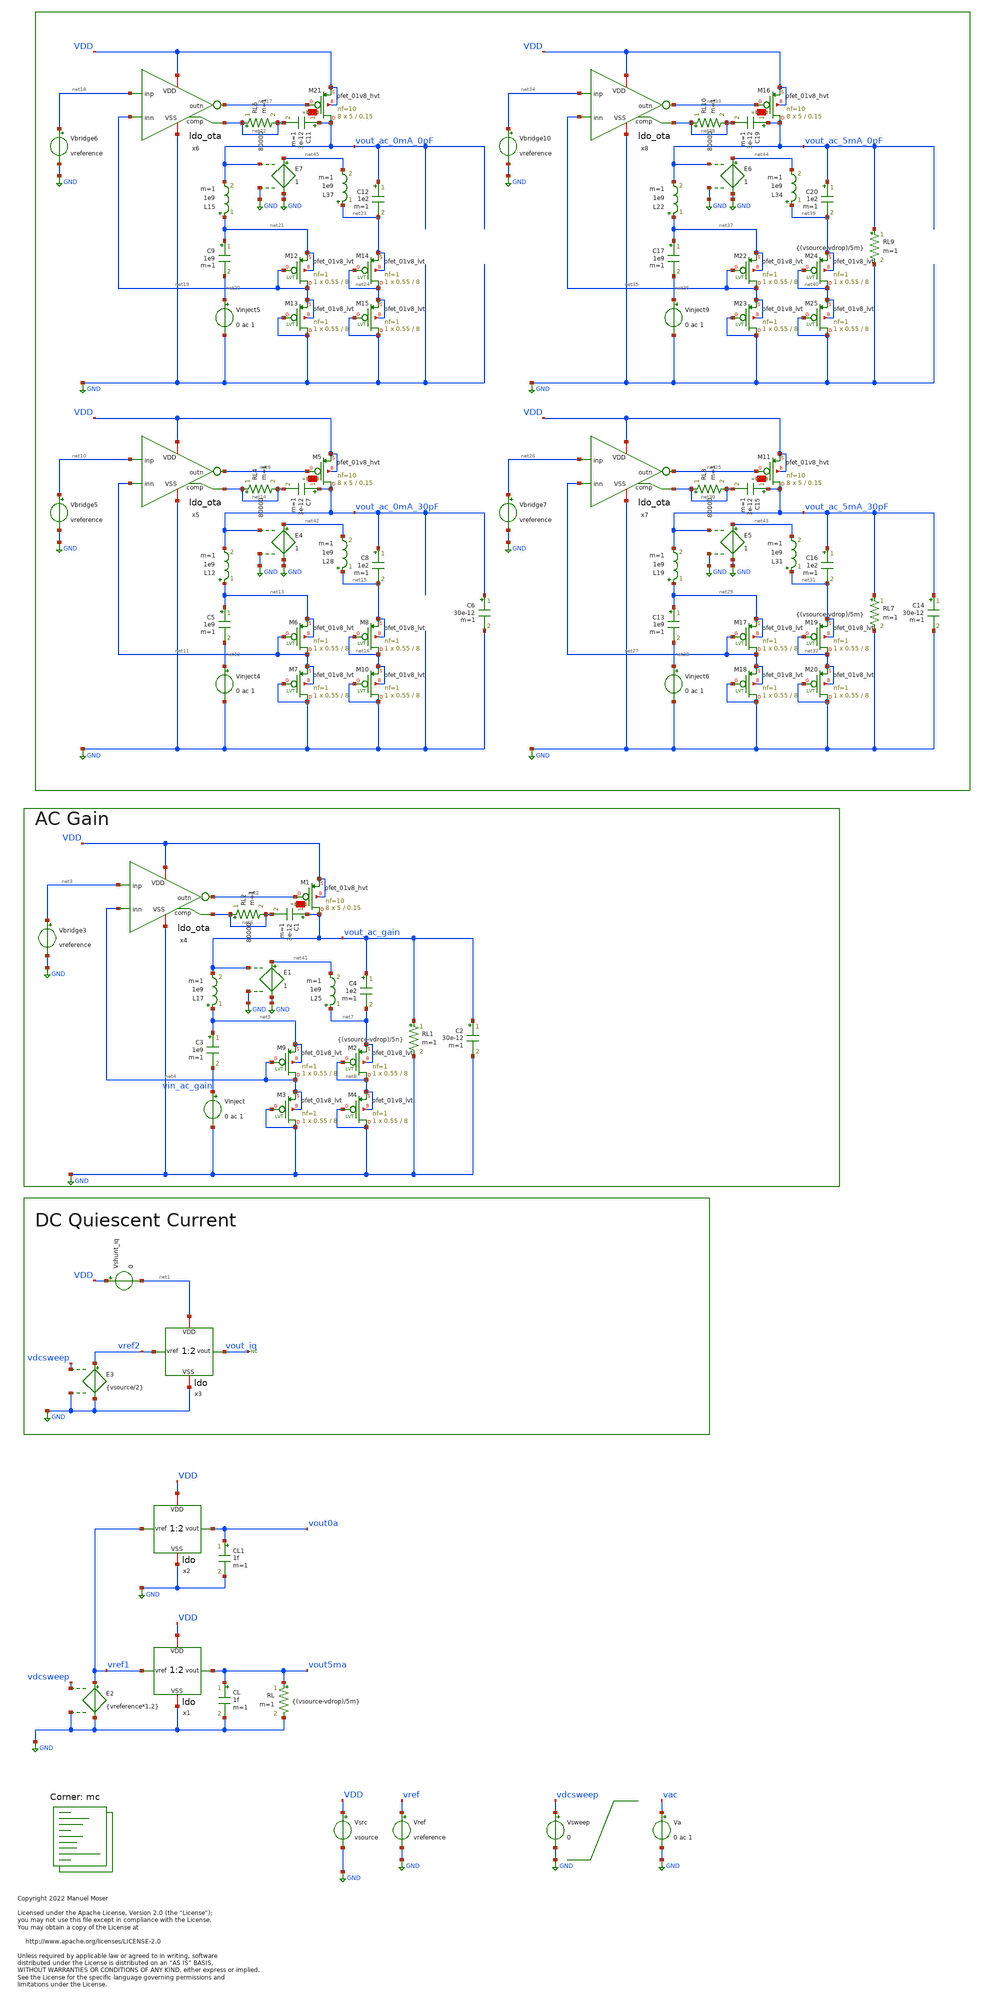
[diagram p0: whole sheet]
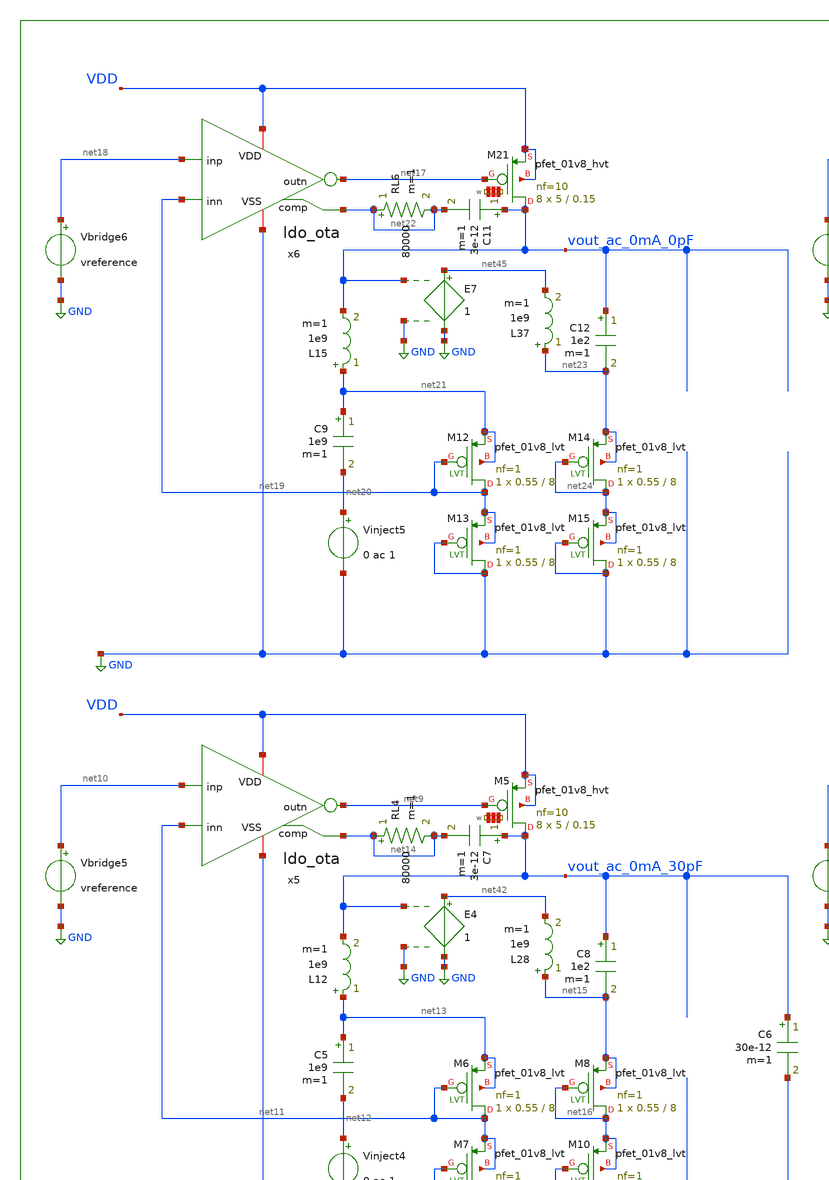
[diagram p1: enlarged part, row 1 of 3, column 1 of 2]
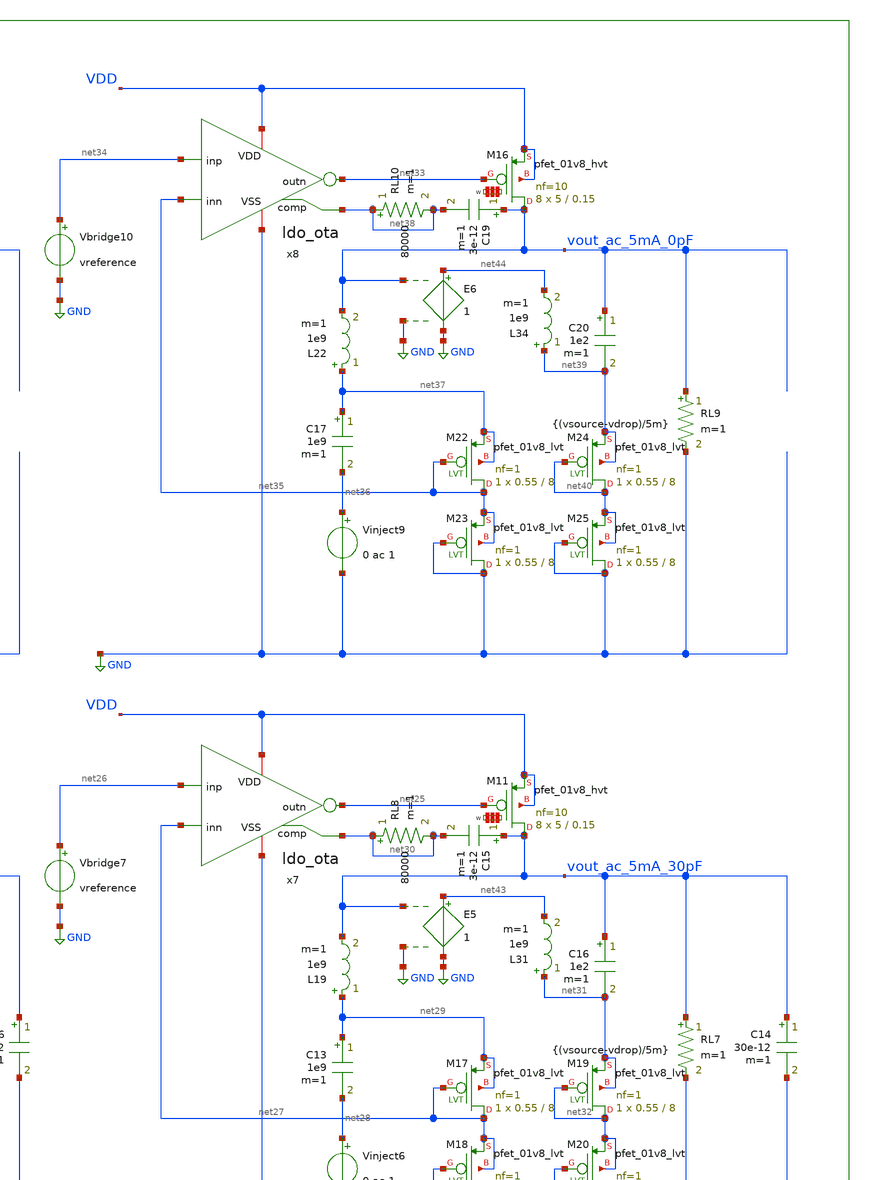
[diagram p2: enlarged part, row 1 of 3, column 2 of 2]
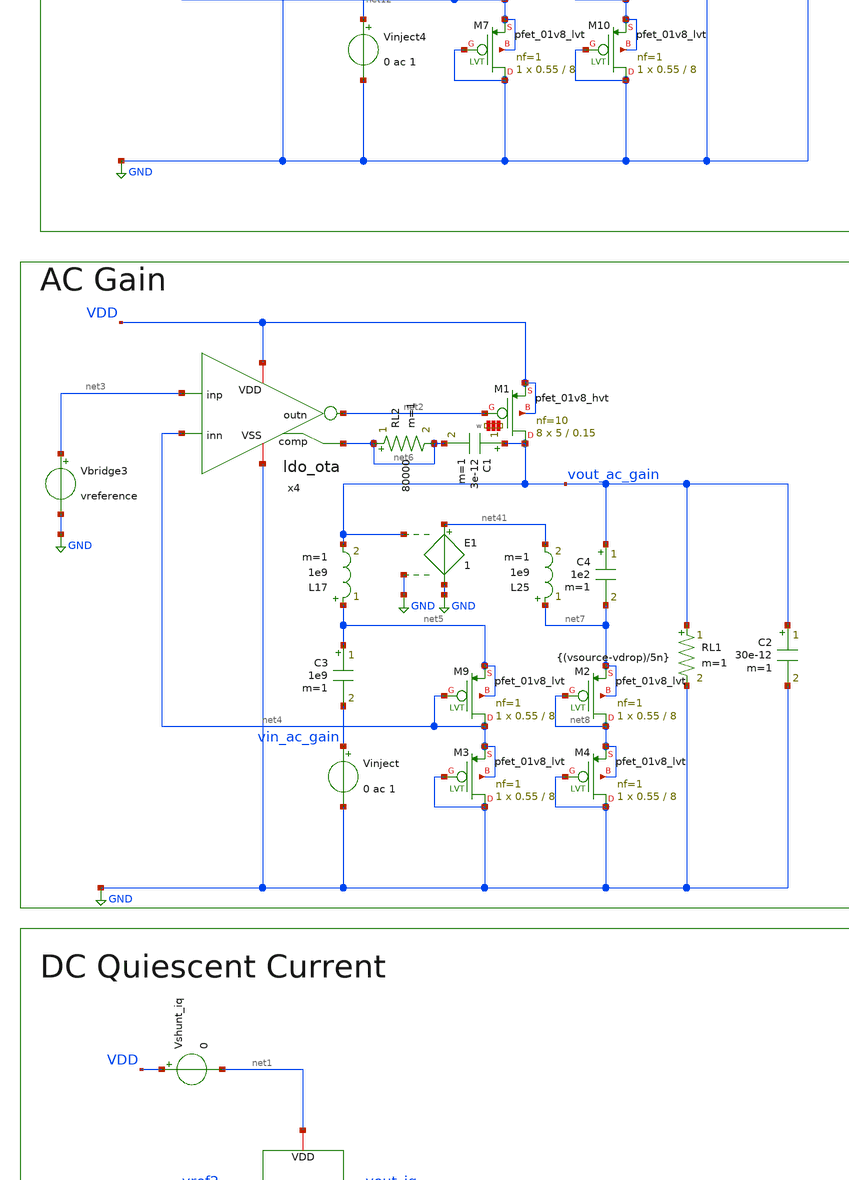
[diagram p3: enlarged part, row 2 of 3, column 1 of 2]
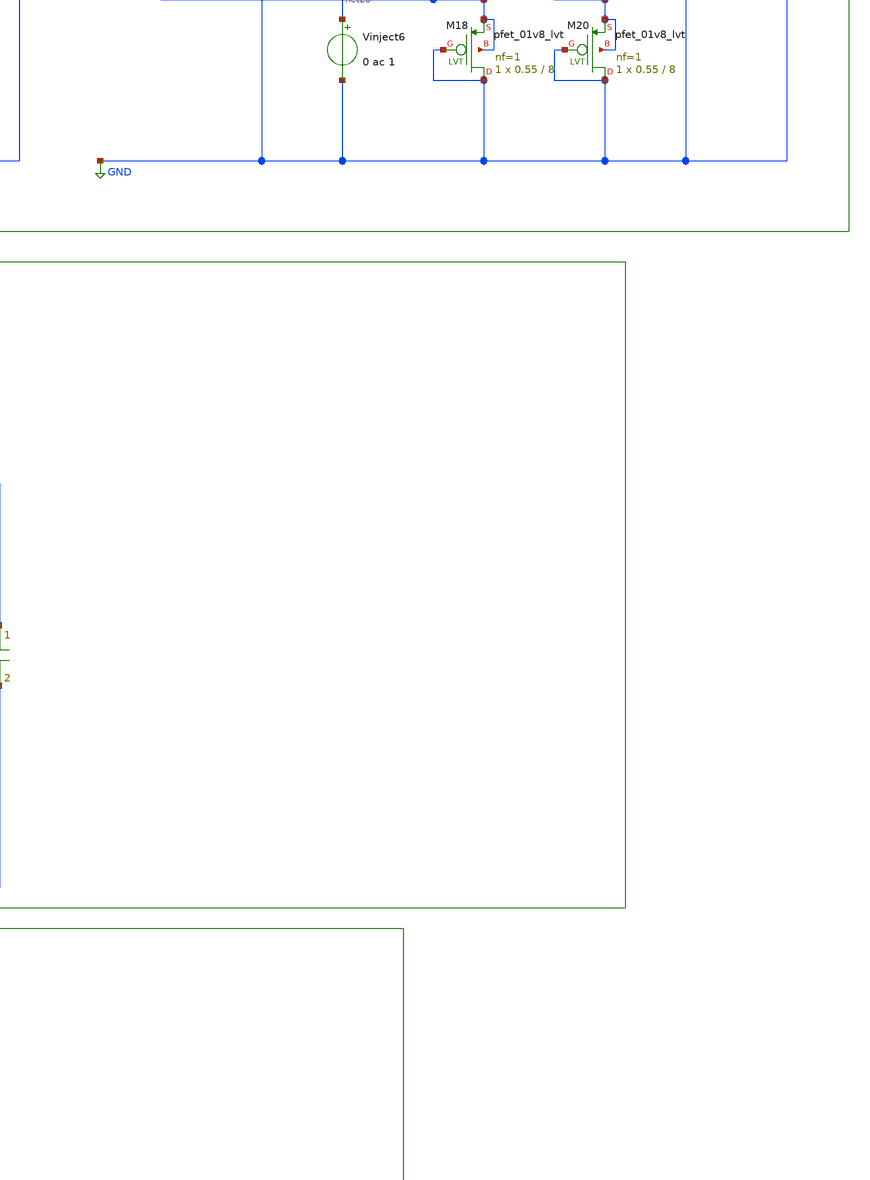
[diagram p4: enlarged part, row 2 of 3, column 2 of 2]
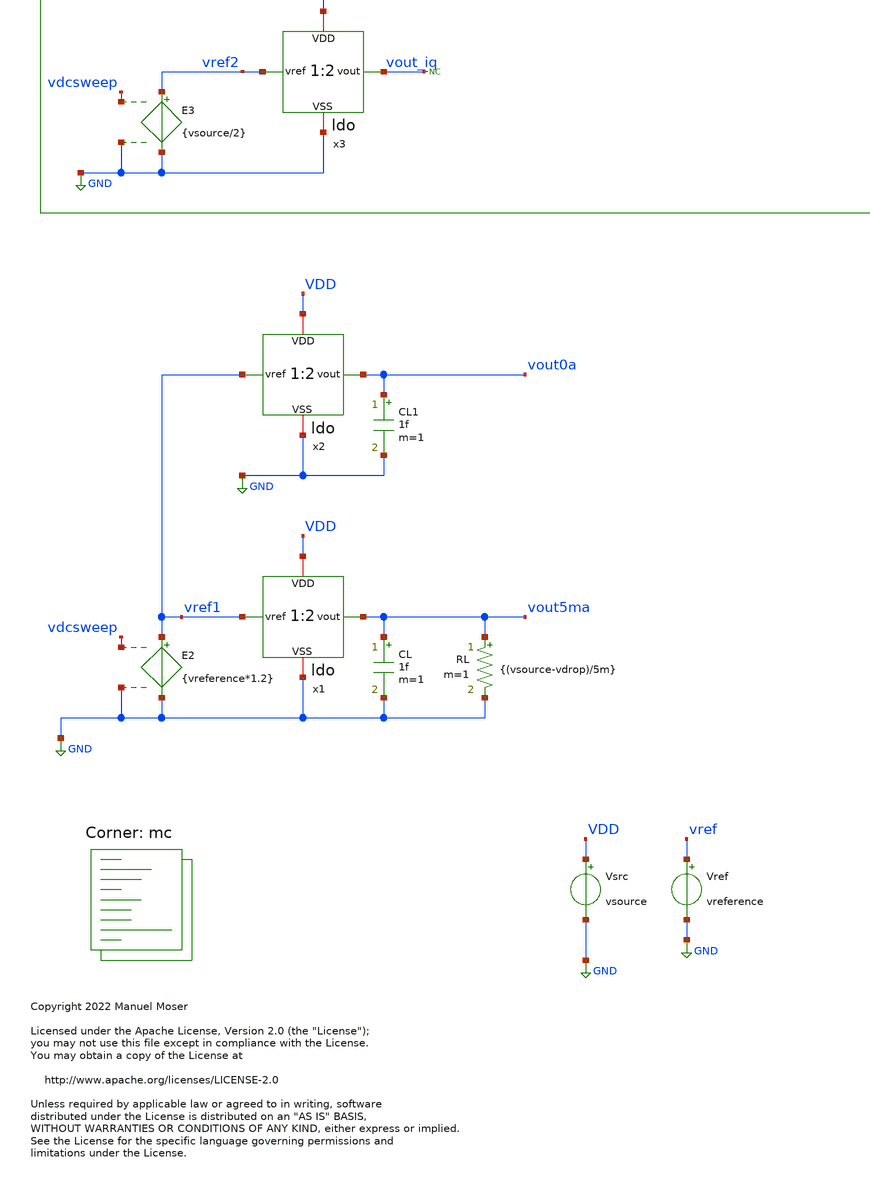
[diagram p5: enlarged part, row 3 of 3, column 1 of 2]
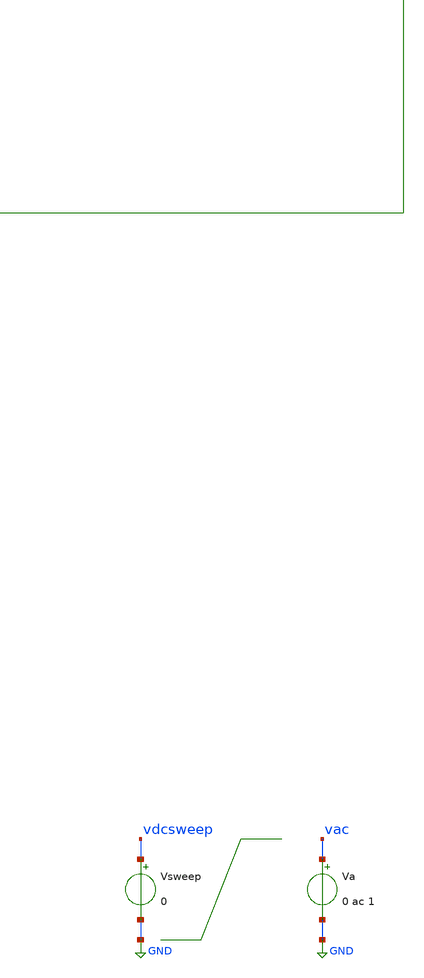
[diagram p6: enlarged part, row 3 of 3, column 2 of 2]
** sch_path: xschem/ldo_tb.sch
* Copyright 2022 Manuel Moser
* Licensed under the Apache License, Version 2.0 (the "License");
**.subckt ldo_tb
Vref vref GND vreference
Vsrc VDD GND vsource
Va vac GND 0 ac 1
CL vout5ma GND 1f m=1
RL vout5ma GND {(vsource-vdrop)/5m} m=1
x1 VDD vref1 vout5ma GND ldo
CL1 vout0a GND 1f m=1
x2 VDD vref1 vout0a GND ldo
Vsweep vdcsweep GND 0
E2 vref1 GND vdcsweep GND {vreference*1.2}
x3 net1 vref2 vout_iq GND ldo
Vshunt_iq VDD net1 0
E3 vref2 GND vdcsweep GND {vsource/2}
* noconn vout_iq
x4 VDD net3 net2 net4 GND net6 ldo_ota
L17 net5 vout_ac_gain 1e9 m=1
C3 net5 vin_ac_gain 1e9 m=1
Vinject vin_ac_gain GND 0 ac 1
Vbridge3 net3 GND vreference
RL1 vout_ac_gain GND {(vsource-vdrop)/5n} m=1
C2 vout_ac_gain GND 30e-12 m=1
C1 vout_ac_gain net6 3e-12 m=1
RL2 net6 net6 80000 m=1
XM9 net4 net4 net5 net5 sky130_fd_pr__pfet_01v8_lvt L=8 W=0.55 nf=1 ad='int((nf+1)/2) * W/nf * 0.29'
+ as='int((nf+2)/2) * W/nf * 0.29' pd='2*int((nf+1)/2) * (W/nf + 0.29)' ps='2*int((nf+2)/2) * (W/nf + 0.29)'
+ nrd='0.29 / W' nrs='0.29 / W' sa=0 sb=0 sd=0 mult=1 m=1
XM3 GND GND net4 net4 sky130_fd_pr__pfet_01v8_lvt L=8 W=0.55 nf=1 ad='int((nf+1)/2) * W/nf * 0.29' as='int((nf+2)/2) * W/nf * 0.29'
+ pd='2*int((nf+1)/2) * (W/nf + 0.29)' ps='2*int((nf+2)/2) * (W/nf + 0.29)' nrd='0.29 / W' nrs='0.29 / W'
+ sa=0 sb=0 sd=0 mult=1 m=1
XM2 net8 net8 net7 net7 sky130_fd_pr__pfet_01v8_lvt L=8 W=0.55 nf=1 ad='int((nf+1)/2) * W/nf * 0.29'
+ as='int((nf+2)/2) * W/nf * 0.29' pd='2*int((nf+1)/2) * (W/nf + 0.29)' ps='2*int((nf+2)/2) * (W/nf + 0.29)'
+ nrd='0.29 / W' nrs='0.29 / W' sa=0 sb=0 sd=0 mult=1 m=1
XM4 GND GND net8 net8 sky130_fd_pr__pfet_01v8_lvt L=8 W=0.55 nf=1 ad='int((nf+1)/2) * W/nf * 0.29' as='int((nf+2)/2) * W/nf * 0.29'
+ pd='2*int((nf+1)/2) * (W/nf + 0.29)' ps='2*int((nf+2)/2) * (W/nf + 0.29)' nrd='0.29 / W' nrs='0.29 / W'
+ sa=0 sb=0 sd=0 mult=1 m=1
C4 vout_ac_gain net7 1e2 m=1
x5 VDD net10 net9 net11 GND net14 ldo_ota
L12 net13 vout_ac_0mA_30pF 1e9 m=1
C5 net13 net12 1e9 m=1
Vinject4 net12 GND 0 ac 1
Vbridge5 net10 GND vreference
C6 vout_ac_0mA_30pF GND 30e-12 m=1
C7 vout_ac_0mA_30pF net14 3e-12 m=1
RL4 net14 net14 80000 m=1
XM6 net11 net11 net13 net13 sky130_fd_pr__pfet_01v8_lvt L=8 W=0.55 nf=1 ad='int((nf+1)/2) * W/nf * 0.29'
+ as='int((nf+2)/2) * W/nf * 0.29' pd='2*int((nf+1)/2) * (W/nf + 0.29)' ps='2*int((nf+2)/2) * (W/nf + 0.29)'
+ nrd='0.29 / W' nrs='0.29 / W' sa=0 sb=0 sd=0 mult=1 m=1
XM7 GND GND net11 net11 sky130_fd_pr__pfet_01v8_lvt L=8 W=0.55 nf=1 ad='int((nf+1)/2) * W/nf * 0.29'
+ as='int((nf+2)/2) * W/nf * 0.29' pd='2*int((nf+1)/2) * (W/nf + 0.29)' ps='2*int((nf+2)/2) * (W/nf + 0.29)'
+ nrd='0.29 / W' nrs='0.29 / W' sa=0 sb=0 sd=0 mult=1 m=1
XM8 net16 net16 net15 net15 sky130_fd_pr__pfet_01v8_lvt L=8 W=0.55 nf=1 ad='int((nf+1)/2) * W/nf * 0.29'
+ as='int((nf+2)/2) * W/nf * 0.29' pd='2*int((nf+1)/2) * (W/nf + 0.29)' ps='2*int((nf+2)/2) * (W/nf + 0.29)'
+ nrd='0.29 / W' nrs='0.29 / W' sa=0 sb=0 sd=0 mult=1 m=1
XM10 GND GND net16 net16 sky130_fd_pr__pfet_01v8_lvt L=8 W=0.55 nf=1 ad='int((nf+1)/2) * W/nf * 0.29'
+ as='int((nf+2)/2) * W/nf * 0.29' pd='2*int((nf+1)/2) * (W/nf + 0.29)' ps='2*int((nf+2)/2) * (W/nf + 0.29)'
+ nrd='0.29 / W' nrs='0.29 / W' sa=0 sb=0 sd=0 mult=1 m=1
C8 vout_ac_0mA_30pF net15 1e2 m=1
x6 VDD net18 net17 net19 GND net22 ldo_ota
L15 net21 vout_ac_0mA_0pF 1e9 m=1
C9 net21 net20 1e9 m=1
Vinject5 net20 GND 0 ac 1
Vbridge6 net18 GND vreference
C11 vout_ac_0mA_0pF net22 3e-12 m=1
RL6 net22 net22 80000 m=1
XM12 net19 net19 net21 net21 sky130_fd_pr__pfet_01v8_lvt L=8 W=0.55 nf=1 ad='int((nf+1)/2) * W/nf * 0.29'
+ as='int((nf+2)/2) * W/nf * 0.29' pd='2*int((nf+1)/2) * (W/nf + 0.29)' ps='2*int((nf+2)/2) * (W/nf + 0.29)'
+ nrd='0.29 / W' nrs='0.29 / W' sa=0 sb=0 sd=0 mult=1 m=1
XM13 GND GND net19 net19 sky130_fd_pr__pfet_01v8_lvt L=8 W=0.55 nf=1 ad='int((nf+1)/2) * W/nf * 0.29'
+ as='int((nf+2)/2) * W/nf * 0.29' pd='2*int((nf+1)/2) * (W/nf + 0.29)' ps='2*int((nf+2)/2) * (W/nf + 0.29)'
+ nrd='0.29 / W' nrs='0.29 / W' sa=0 sb=0 sd=0 mult=1 m=1
XM14 net24 net24 net23 net23 sky130_fd_pr__pfet_01v8_lvt L=8 W=0.55 nf=1 ad='int((nf+1)/2) * W/nf * 0.29'
+ as='int((nf+2)/2) * W/nf * 0.29' pd='2*int((nf+1)/2) * (W/nf + 0.29)' ps='2*int((nf+2)/2) * (W/nf + 0.29)'
+ nrd='0.29 / W' nrs='0.29 / W' sa=0 sb=0 sd=0 mult=1 m=1
XM15 GND GND net24 net24 sky130_fd_pr__pfet_01v8_lvt L=8 W=0.55 nf=1 ad='int((nf+1)/2) * W/nf * 0.29'
+ as='int((nf+2)/2) * W/nf * 0.29' pd='2*int((nf+1)/2) * (W/nf + 0.29)' ps='2*int((nf+2)/2) * (W/nf + 0.29)'
+ nrd='0.29 / W' nrs='0.29 / W' sa=0 sb=0 sd=0 mult=1 m=1
C12 vout_ac_0mA_0pF net23 1e2 m=1
x7 VDD net26 net25 net27 GND net30 ldo_ota
L19 net29 vout_ac_5mA_30pF 1e9 m=1
C13 net29 net28 1e9 m=1
Vinject6 net28 GND 0 ac 1
Vbridge7 net26 GND vreference
RL7 vout_ac_5mA_30pF GND {(vsource-vdrop)/5m} m=1
C14 vout_ac_5mA_30pF GND 30e-12 m=1
C15 vout_ac_5mA_30pF net30 3e-12 m=1
RL8 net30 net30 80000 m=1
XM17 net27 net27 net29 net29 sky130_fd_pr__pfet_01v8_lvt L=8 W=0.55 nf=1 ad='int((nf+1)/2) * W/nf * 0.29'
+ as='int((nf+2)/2) * W/nf * 0.29' pd='2*int((nf+1)/2) * (W/nf + 0.29)' ps='2*int((nf+2)/2) * (W/nf + 0.29)'
+ nrd='0.29 / W' nrs='0.29 / W' sa=0 sb=0 sd=0 mult=1 m=1
XM18 GND GND net27 net27 sky130_fd_pr__pfet_01v8_lvt L=8 W=0.55 nf=1 ad='int((nf+1)/2) * W/nf * 0.29'
+ as='int((nf+2)/2) * W/nf * 0.29' pd='2*int((nf+1)/2) * (W/nf + 0.29)' ps='2*int((nf+2)/2) * (W/nf + 0.29)'
+ nrd='0.29 / W' nrs='0.29 / W' sa=0 sb=0 sd=0 mult=1 m=1
XM19 net32 net32 net31 net31 sky130_fd_pr__pfet_01v8_lvt L=8 W=0.55 nf=1 ad='int((nf+1)/2) * W/nf * 0.29'
+ as='int((nf+2)/2) * W/nf * 0.29' pd='2*int((nf+1)/2) * (W/nf + 0.29)' ps='2*int((nf+2)/2) * (W/nf + 0.29)'
+ nrd='0.29 / W' nrs='0.29 / W' sa=0 sb=0 sd=0 mult=1 m=1
XM20 GND GND net32 net32 sky130_fd_pr__pfet_01v8_lvt L=8 W=0.55 nf=1 ad='int((nf+1)/2) * W/nf * 0.29'
+ as='int((nf+2)/2) * W/nf * 0.29' pd='2*int((nf+1)/2) * (W/nf + 0.29)' ps='2*int((nf+2)/2) * (W/nf + 0.29)'
+ nrd='0.29 / W' nrs='0.29 / W' sa=0 sb=0 sd=0 mult=1 m=1
C16 vout_ac_5mA_30pF net31 1e2 m=1
x8 VDD net34 net33 net35 GND net38 ldo_ota
L22 net37 vout_ac_5mA_0pF 1e9 m=1
C17 net37 net36 1e9 m=1
Vinject9 net36 GND 0 ac 1
Vbridge10 net34 GND vreference
RL9 vout_ac_5mA_0pF GND {(vsource-vdrop)/5m} m=1
C19 vout_ac_5mA_0pF net38 3e-12 m=1
RL10 net38 net38 80000 m=1
XM22 net35 net35 net37 net37 sky130_fd_pr__pfet_01v8_lvt L=8 W=0.55 nf=1 ad='int((nf+1)/2) * W/nf * 0.29'
+ as='int((nf+2)/2) * W/nf * 0.29' pd='2*int((nf+1)/2) * (W/nf + 0.29)' ps='2*int((nf+2)/2) * (W/nf + 0.29)'
+ nrd='0.29 / W' nrs='0.29 / W' sa=0 sb=0 sd=0 mult=1 m=1
XM23 GND GND net35 net35 sky130_fd_pr__pfet_01v8_lvt L=8 W=0.55 nf=1 ad='int((nf+1)/2) * W/nf * 0.29'
+ as='int((nf+2)/2) * W/nf * 0.29' pd='2*int((nf+1)/2) * (W/nf + 0.29)' ps='2*int((nf+2)/2) * (W/nf + 0.29)'
+ nrd='0.29 / W' nrs='0.29 / W' sa=0 sb=0 sd=0 mult=1 m=1
XM24 net40 net40 net39 net39 sky130_fd_pr__pfet_01v8_lvt L=8 W=0.55 nf=1 ad='int((nf+1)/2) * W/nf * 0.29'
+ as='int((nf+2)/2) * W/nf * 0.29' pd='2*int((nf+1)/2) * (W/nf + 0.29)' ps='2*int((nf+2)/2) * (W/nf + 0.29)'
+ nrd='0.29 / W' nrs='0.29 / W' sa=0 sb=0 sd=0 mult=1 m=1
XM25 GND GND net40 net40 sky130_fd_pr__pfet_01v8_lvt L=8 W=0.55 nf=1 ad='int((nf+1)/2) * W/nf * 0.29'
+ as='int((nf+2)/2) * W/nf * 0.29' pd='2*int((nf+1)/2) * (W/nf + 0.29)' ps='2*int((nf+2)/2) * (W/nf + 0.29)'
+ nrd='0.29 / W' nrs='0.29 / W' sa=0 sb=0 sd=0 mult=1 m=1
C20 vout_ac_5mA_0pF net39 1e2 m=1
L25 net7 net41 1e9 m=1
E1 net41 GND vout_ac_gain GND 1
L28 net15 net42 1e9 m=1
E4 net42 GND vout_ac_0mA_30pF GND 1
L31 net31 net43 1e9 m=1
E5 net43 GND vout_ac_5mA_30pF GND 1
L34 net39 net44 1e9 m=1
E6 net44 GND vout_ac_5mA_0pF GND 1
L37 net23 net45 1e9 m=1
E7 net45 GND vout_ac_0mA_0pF GND 1
XM1 vout_ac_gain net2 VDD VDD sky130_fd_pr__pfet_01v8_hvt L=0.15 W='5 * 10 ' nf=10 ad='int((nf+1)/2) * W / nf * 0.29'
+ as='int((nf+2)/2) * W / nf * 0.29' pd='2*int((nf+1)/2) * (W / nf + 0.29)' ps='2*int((nf+2)/2) * (W / nf + 0.29)'
+ nrd='0.29 / W ' nrs='0.29 / W ' sa=0 sb=0 sd=0 mult=8 m=8
XM5 vout_ac_0mA_30pF net9 VDD VDD sky130_fd_pr__pfet_01v8_hvt L=0.15 W='5 * 10 ' nf=10 ad='int((nf+1)/2) * W / nf * 0.29'
+ as='int((nf+2)/2) * W / nf * 0.29' pd='2*int((nf+1)/2) * (W / nf + 0.29)' ps='2*int((nf+2)/2) * (W / nf + 0.29)'
+ nrd='0.29 / W ' nrs='0.29 / W ' sa=0 sb=0 sd=0 mult=8 m=8
XM11 vout_ac_5mA_30pF net25 VDD VDD sky130_fd_pr__pfet_01v8_hvt L=0.15 W='5 * 10 ' nf=10 ad='int((nf+1)/2) * W / nf * 0.29'
+ as='int((nf+2)/2) * W / nf * 0.29' pd='2*int((nf+1)/2) * (W / nf + 0.29)' ps='2*int((nf+2)/2) * (W / nf + 0.29)'
+ nrd='0.29 / W ' nrs='0.29 / W ' sa=0 sb=0 sd=0 mult=8 m=8
XM16 vout_ac_5mA_0pF net33 VDD VDD sky130_fd_pr__pfet_01v8_hvt L=0.15 W='5 * 10 ' nf=10 ad='int((nf+1)/2) * W / nf * 0.29'
+ as='int((nf+2)/2) * W / nf * 0.29' pd='2*int((nf+1)/2) * (W / nf + 0.29)' ps='2*int((nf+2)/2) * (W / nf + 0.29)'
+ nrd='0.29 / W ' nrs='0.29 / W ' sa=0 sb=0 sd=0 mult=8 m=8
XM21 vout_ac_0mA_0pF net17 VDD VDD sky130_fd_pr__pfet_01v8_hvt L=0.15 W='5 * 10 ' nf=10 ad='int((nf+1)/2) * W / nf * 0.29'
+ as='int((nf+2)/2) * W / nf * 0.29' pd='2*int((nf+1)/2) * (W / nf + 0.29)' ps='2*int((nf+2)/2) * (W / nf + 0.29)'
+ nrd='0.29 / W ' nrs='0.29 / W ' sa=0 sb=0 sd=0 mult=8 m=8
**** begin user architecture code



.temp 27
*.option gmin = 1e-16
.option RSHUNT=1E15
.option method = gear

.param vsource = 1.80
.param vdrop = 0.20
.param vreference = {(vsource-vdrop)/2}

.save all
.options savecurrents

.control
set num_threads = 12
write results_ldo.raw
set appendwrite

repeat 10
reset

dc vsweep 0 1 0.01 temp -30 60 90
*dc vsweep 0 1 0.01
write results_ldo.raw   vref1 vout5ma vout0a x1.vota x1.vfb
+ @m.x1.xm9.msky130_fd_pr__pfet_01v8_lvt[id]  vref2 i(vshunt_iq) vout_ac_gain

ac dec 10 1 10meg
write results_ldo.raw vout_ac_0mA_0pF vout_ac_0mA_30pF vout_ac_5mA_0pF vout_ac_5mA_30pF

*pz vinject gnd vout_ac_gain gnd vol pz


end

.endc




.lib $::SKYWATER_MODELS/sky130.lib.spice mc
**** end user architecture code
**.ends

* expanding   symbol:  ldo.sym # of pins=4
** sym_path: xschem/ldo.sym
** sch_path: xschem/ldo.sch
.subckt ldo VDD vref vout VSS
*.ipin vref
*.iopin VDD
*.iopin VSS
*.opin vout
x1 VDD vref vota vfb VSS net1 ldo_ota
XM1 vout vota VDD VDD sky130_fd_pr__pfet_01v8 L=0.15 W='5 * 5 ' nf=5 ad='int((nf+1)/2) * W / nf * 0.29'
+ as='int((nf+2)/2) * W / nf * 0.29' pd='2*int((nf+1)/2) * (W / nf + 0.29)' ps='2*int((nf+2)/2) * (W / nf + 0.29)'
+ nrd='0.29 / W ' nrs='0.29 / W ' sa=0 sb=0 sd=0 mult=14 m=14
C1 vout net2 3e-12 m=1
RL2 net1 net2 80000 m=1
XM9 vfb vfb vout vout sky130_fd_pr__pfet_01v8_lvt L=8 W=0.55 nf=1 ad='int((nf+1)/2) * W/nf * 0.29' as='int((nf+2)/2) * W/nf * 0.29'
+ pd='2*int((nf+1)/2) * (W/nf + 0.29)' ps='2*int((nf+2)/2) * (W/nf + 0.29)' nrd='0.29 / W' nrs='0.29 / W'
+ sa=0 sb=0 sd=0 mult=1 m=1
XM3 VSS VSS vfb vfb sky130_fd_pr__pfet_01v8_lvt L=8 W=0.55 nf=1 ad='int((nf+1)/2) * W/nf * 0.29' as='int((nf+2)/2) * W/nf * 0.29'
+ pd='2*int((nf+1)/2) * (W/nf + 0.29)' ps='2*int((nf+2)/2) * (W/nf + 0.29)' nrd='0.29 / W' nrs='0.29 / W'
+ sa=0 sb=0 sd=0 mult=1 m=1
.ends


* expanding   symbol:  ldo_ota.sym # of pins=6
** sym_path: xschem/ldo_ota.sym
** sch_path: xschem/ldo_ota.sch
.subckt ldo_ota VDD inp outn inn VSS comp
*.iopin VDD
*.iopin VSS
*.ipin inp
*.ipin inn
*.opin outn
*.opin comp
x2 bias2 VDD VSS bias1 ldo_isource
XM10 net1 bias2 VDD VDD sky130_fd_pr__pfet_01v8_lvt L=8 W='0.55 * 1 ' nf=1 ad='int((nf+1)/2) * W / nf * 0.29'
+ as='int((nf+2)/2) * W / nf * 0.29' pd='2*int((nf+1)/2) * (W / nf + 0.29)' ps='2*int((nf+2)/2) * (W / nf + 0.29)'
+ nrd='0.29 / W ' nrs='0.29 / W ' sa=0 sb=0 sd=0 mult=1 m=1
XM12 bias2 bias2 net1 VDD sky130_fd_pr__pfet_01v8_lvt L=8 W='0.55 * 4 ' nf=4 ad='int((nf+1)/2) * W / nf * 0.29'
+ as='int((nf+2)/2) * W / nf * 0.29' pd='2*int((nf+1)/2) * (W / nf + 0.29)' ps='2*int((nf+2)/2) * (W / nf + 0.29)'
+ nrd='0.29 / W ' nrs='0.29 / W ' sa=0 sb=0 sd=0 mult=1 m=1
XM1 net2 bias1 VDD VDD sky130_fd_pr__pfet_01v8_lvt L=8 W='0.55 * 4 ' nf=4 ad='int((nf+1)/2) * W / nf * 0.29'
+ as='int((nf+2)/2) * W / nf * 0.29' pd='2*int((nf+1)/2) * (W / nf + 0.29)' ps='2*int((nf+2)/2) * (W / nf + 0.29)'
+ nrd='0.29 / W ' nrs='0.29 / W ' sa=0 sb=0 sd=0 mult=1 m=1
XM2 bias1 bias2 net2 VDD sky130_fd_pr__pfet_01v8_lvt L=8 W='0.55 * 4 ' nf=4 ad='int((nf+1)/2) * W / nf * 0.29'
+ as='int((nf+2)/2) * W / nf * 0.29' pd='2*int((nf+1)/2) * (W / nf + 0.29)' ps='2*int((nf+2)/2) * (W / nf + 0.29)'
+ nrd='0.29 / W ' nrs='0.29 / W ' sa=0 sb=0 sd=0 mult=1 m=1
XM3 net3 bias1 VDD VDD sky130_fd_pr__pfet_01v8_lvt L=8 W='0.55 * 4 ' nf=4 ad='int((nf+1)/2) * W / nf * 0.29'
+ as='int((nf+2)/2) * W / nf * 0.29' pd='2*int((nf+1)/2) * (W / nf + 0.29)' ps='2*int((nf+2)/2) * (W / nf + 0.29)'
+ nrd='0.29 / W ' nrs='0.29 / W ' sa=0 sb=0 sd=0 mult=1 m=1
XM4 bias3 bias2 net3 VDD sky130_fd_pr__pfet_01v8_lvt L=8 W='0.55 * 4 ' nf=4 ad='int((nf+1)/2) * W / nf * 0.29'
+ as='int((nf+2)/2) * W / nf * 0.29' pd='2*int((nf+1)/2) * (W / nf + 0.29)' ps='2*int((nf+2)/2) * (W / nf + 0.29)'
+ nrd='0.29 / W ' nrs='0.29 / W ' sa=0 sb=0 sd=0 mult=1 m=1
XM5 net4 bias1 VDD VDD sky130_fd_pr__pfet_01v8_lvt L=8 W='0.55 * 4 ' nf=4 ad='int((nf+1)/2) * W / nf * 0.29'
+ as='int((nf+2)/2) * W / nf * 0.29' pd='2*int((nf+1)/2) * (W / nf + 0.29)' ps='2*int((nf+2)/2) * (W / nf + 0.29)'
+ nrd='0.29 / W ' nrs='0.29 / W ' sa=0 sb=0 sd=0 mult=1 m=1
XM8 bias4 bias2 net4 VDD sky130_fd_pr__pfet_01v8_lvt L=8 W='0.55 * 4 ' nf=4 ad='int((nf+1)/2) * W / nf * 0.29'
+ as='int((nf+2)/2) * W / nf * 0.29' pd='2*int((nf+1)/2) * (W / nf + 0.29)' ps='2*int((nf+2)/2) * (W / nf + 0.29)'
+ nrd='0.29 / W ' nrs='0.29 / W ' sa=0 sb=0 sd=0 mult=1 m=1
XM9 bias3 bias3 net5 VSS sky130_fd_pr__nfet_01v8_lvt L=4 W='1 * 2 ' nf=2 ad='int((nf+1)/2) * W / nf * 0.29'
+ as='int((nf+2)/2) * W / nf * 0.29' pd='2*int((nf+1)/2) * (W / nf + 0.29)' ps='2*int((nf+2)/2) * (W / nf + 0.29)'
+ nrd='0.29 / W ' nrs='0.29 / W ' sa=0 sb=0 sd=0 mult=1 m=1
XM11 net5 bias3 net10 VSS sky130_fd_pr__nfet_01v8 L=8 W='0.42 * 1 ' nf=1 ad='int((nf+1)/2) * W / nf * 0.29'
+ as='int((nf+2)/2) * W / nf * 0.29' pd='2*int((nf+1)/2) * (W / nf + 0.29)' ps='2*int((nf+2)/2) * (W / nf + 0.29)'
+ nrd='0.29 / W ' nrs='0.29 / W ' sa=0 sb=0 sd=0 mult=1 m=1
XM13 bias4 bias3 net6 VSS sky130_fd_pr__nfet_01v8_lvt L=4 W='1 * 2 ' nf=2 ad='int((nf+1)/2) * W / nf * 0.29'
+ as='int((nf+2)/2) * W / nf * 0.29' pd='2*int((nf+1)/2) * (W / nf + 0.29)' ps='2*int((nf+2)/2) * (W / nf + 0.29)'
+ nrd='0.29 / W ' nrs='0.29 / W ' sa=0 sb=0 sd=0 mult=1 m=1
XM14 net6 bias4 net7 VSS sky130_fd_pr__nfet_01v8 L=8 W='0.42 * 4 ' nf=4 ad='int((nf+1)/2) * W / nf * 0.29'
+ as='int((nf+2)/2) * W / nf * 0.29' pd='2*int((nf+1)/2) * (W / nf + 0.29)' ps='2*int((nf+2)/2) * (W / nf + 0.29)'
+ nrd='0.29 / W ' nrs='0.29 / W ' sa=0 sb=0 sd=0 mult=1 m=1
XM6 net7 bias4 net8 VSS sky130_fd_pr__nfet_01v8 L=8 W='0.42 * 4 ' nf=4 ad='int((nf+1)/2) * W / nf * 0.29'
+ as='int((nf+2)/2) * W / nf * 0.29' pd='2*int((nf+1)/2) * (W / nf + 0.29)' ps='2*int((nf+2)/2) * (W / nf + 0.29)'
+ nrd='0.29 / W ' nrs='0.29 / W ' sa=0 sb=0 sd=0 mult=1 m=1
XM7 net10 bias3 net9 VSS sky130_fd_pr__nfet_01v8 L=8 W='0.42 * 1 ' nf=1 ad='int((nf+1)/2) * W / nf * 0.29'
+ as='int((nf+2)/2) * W / nf * 0.29' pd='2*int((nf+1)/2) * (W / nf + 0.29)' ps='2*int((nf+2)/2) * (W / nf + 0.29)'
+ nrd='0.29 / W ' nrs='0.29 / W ' sa=0 sb=0 sd=0 mult=1 m=1
x1 VDD inp inn bias1 bias2 bias3 outn VSS bias4 comp ldo_fc_n
XM15 net9 bias3 net11 VSS sky130_fd_pr__nfet_01v8 L=8 W='0.42 * 1 ' nf=1 ad='int((nf+1)/2) * W / nf * 0.29'
+ as='int((nf+2)/2) * W / nf * 0.29' pd='2*int((nf+1)/2) * (W / nf + 0.29)' ps='2*int((nf+2)/2) * (W / nf + 0.29)'
+ nrd='0.29 / W ' nrs='0.29 / W ' sa=0 sb=0 sd=0 mult=1 m=1
XM16 net8 bias4 net12 VSS sky130_fd_pr__nfet_01v8 L=8 W='0.42 * 4 ' nf=4 ad='int((nf+1)/2) * W / nf * 0.29'
+ as='int((nf+2)/2) * W / nf * 0.29' pd='2*int((nf+1)/2) * (W / nf + 0.29)' ps='2*int((nf+2)/2) * (W / nf + 0.29)'
+ nrd='0.29 / W ' nrs='0.29 / W ' sa=0 sb=0 sd=0 mult=1 m=1
XM17 net12 bias4 VSS VSS sky130_fd_pr__nfet_01v8 L=8 W='0.42 * 4 ' nf=4 ad='int((nf+1)/2) * W / nf * 0.29'
+ as='int((nf+2)/2) * W / nf * 0.29' pd='2*int((nf+1)/2) * (W / nf + 0.29)' ps='2*int((nf+2)/2) * (W / nf + 0.29)'
+ nrd='0.29 / W ' nrs='0.29 / W ' sa=0 sb=0 sd=0 mult=1 m=1
XM18 net11 bias3 VSS VSS sky130_fd_pr__nfet_01v8 L=8 W='0.42 * 1 ' nf=1 ad='int((nf+1)/2) * W / nf * 0.29'
+ as='int((nf+2)/2) * W / nf * 0.29' pd='2*int((nf+1)/2) * (W / nf + 0.29)' ps='2*int((nf+2)/2) * (W / nf + 0.29)'
+ nrd='0.29 / W ' nrs='0.29 / W ' sa=0 sb=0 sd=0 mult=1 m=1
.ends


* expanding   symbol:  ldo_isource.sym # of pins=4
** sym_path: xschem/ldo_isource.sym
** sch_path: xschem/ldo_isource.sch
.subckt ldo_isource curr_n1 VDD VSS curr_n2
*.iopin VDD
*.iopin VSS
*.ipin curr_n1
*.ipin curr_n2
XMP2 VGP VGP net4 VDD sky130_fd_pr__pfet_01v8_lvt L=8 W='0.55 * 7 ' nf=7 ad='int((nf+1)/2) * W / nf * 0.29'
+ as='int((nf+2)/2) * W / nf * 0.29' pd='2*int((nf+1)/2) * (W / nf + 0.29)' ps='2*int((nf+2)/2) * (W / nf + 0.29)'
+ nrd='0.29 / W ' nrs='0.29 / W ' sa=0 sb=0 sd=0 mult=1 m=1
XMP1 VGN VGP net3 VDD sky130_fd_pr__pfet_01v8_lvt L=8 W='0.55 * 7 ' nf=7 ad='int((nf+1)/2) * W / nf * 0.29'
+ as='int((nf+2)/2) * W / nf * 0.29' pd='2*int((nf+1)/2) * (W / nf + 0.29)' ps='2*int((nf+2)/2) * (W / nf + 0.29)'
+ nrd='0.29 / W ' nrs='0.29 / W ' sa=0 sb=0 sd=0 mult=1 m=1
XMN1 VGN VGN net1 VSS sky130_fd_pr__nfet_01v8_lvt L=8 W='7 * 1 ' nf=1 ad='int((nf+1)/2) * W / nf * 0.29'
+ as='int((nf+2)/2) * W / nf * 0.29' pd='2*int((nf+1)/2) * (W / nf + 0.29)' ps='2*int((nf+2)/2) * (W / nf + 0.29)'
+ nrd='0.29 / W ' nrs='0.29 / W ' sa=0 sb=0 sd=0 mult=1 m=1
XMN2 VGP VGN net2 VSS sky130_fd_pr__nfet_01v8_lvt L=8 W='7 * 1 ' nf=1 ad='int((nf+1)/2) * W / nf * 0.29'
+ as='int((nf+2)/2) * W / nf * 0.29' pd='2*int((nf+1)/2) * (W / nf + 0.29)' ps='2*int((nf+2)/2) * (W / nf + 0.29)'
+ nrd='0.29 / W ' nrs='0.29 / W ' sa=0 sb=0 sd=0 mult=5 m=5
XMN3 net1 VGN VSS VSS sky130_fd_pr__nfet_01v8_lvt L=8 W='7 * 1 ' nf=1 ad='int((nf+1)/2) * W / nf * 0.29'
+ as='int((nf+2)/2) * W / nf * 0.29' pd='2*int((nf+1)/2) * (W / nf + 0.29)' ps='2*int((nf+2)/2) * (W / nf + 0.29)'
+ nrd='0.29 / W ' nrs='0.29 / W ' sa=0 sb=0 sd=0 mult=1 m=1
XMN4 net2 VGN Vref VSS sky130_fd_pr__nfet_01v8_lvt L=8 W='7 * 1 ' nf=1 ad='int((nf+1)/2) * W / nf * 0.29'
+ as='int((nf+2)/2) * W / nf * 0.29' pd='2*int((nf+1)/2) * (W / nf + 0.29)' ps='2*int((nf+2)/2) * (W / nf + 0.29)'
+ nrd='0.29 / W ' nrs='0.29 / W ' sa=0 sb=0 sd=0 mult=5 m=5
XMP4 net3 VGP VDD VDD sky130_fd_pr__pfet_01v8_lvt L=8 W='0.55 * 7 ' nf=7 ad='int((nf+1)/2) * W / nf * 0.29'
+ as='int((nf+2)/2) * W / nf * 0.29' pd='2*int((nf+1)/2) * (W / nf + 0.29)' ps='2*int((nf+2)/2) * (W / nf + 0.29)'
+ nrd='0.29 / W ' nrs='0.29 / W ' sa=0 sb=0 sd=0 mult=1 m=1
XMP5 net4 VGP VDD VDD sky130_fd_pr__pfet_01v8_lvt L=8 W='0.55 * 7 ' nf=7 ad='int((nf+1)/2) * W / nf * 0.29'
+ as='int((nf+2)/2) * W / nf * 0.29' pd='2*int((nf+1)/2) * (W / nf + 0.29)' ps='2*int((nf+2)/2) * (W / nf + 0.29)'
+ nrd='0.29 / W ' nrs='0.29 / W ' sa=0 sb=0 sd=0 mult=1 m=1
XMP3 Vrefgate VGP net19 VDD sky130_fd_pr__pfet_01v8_lvt L=8 W='0.55 * 7 ' nf=7 ad='int((nf+1)/2) * W / nf * 0.29'
+ as='int((nf+2)/2) * W / nf * 0.29' pd='2*int((nf+1)/2) * (W / nf + 0.29)' ps='2*int((nf+2)/2) * (W / nf + 0.29)'
+ nrd='0.29 / W ' nrs='0.29 / W ' sa=0 sb=0 sd=0 mult=1 m=1
XM2 net5 Vrefgate net6 VSS sky130_fd_pr__nfet_01v8 L=4 W='1 * 1 ' nf=1 ad='int((nf+1)/2) * W / nf * 0.29'
+ as='int((nf+2)/2) * W / nf * 0.29' pd='2*int((nf+1)/2) * (W / nf + 0.29)' ps='2*int((nf+2)/2) * (W / nf + 0.29)'
+ nrd='0.29 / W ' nrs='0.29 / W ' sa=0 sb=0 sd=0 mult=1 m=1
XM3 net8 Vrefgate VSS VSS sky130_fd_pr__nfet_01v8 L=4 W='1 * 1 ' nf=1 ad='int((nf+1)/2) * W / nf * 0.29'
+ as='int((nf+2)/2) * W / nf * 0.29' pd='2*int((nf+1)/2) * (W / nf + 0.29)' ps='2*int((nf+2)/2) * (W / nf + 0.29)'
+ nrd='0.29 / W ' nrs='0.29 / W ' sa=0 sb=0 sd=0 mult=1 m=1
XM1 net7 Vrefgate net8 VSS sky130_fd_pr__nfet_01v8 L=4 W='1 * 1 ' nf=1 ad='int((nf+1)/2) * W / nf * 0.29'
+ as='int((nf+2)/2) * W / nf * 0.29' pd='2*int((nf+1)/2) * (W / nf + 0.29)' ps='2*int((nf+2)/2) * (W / nf + 0.29)'
+ nrd='0.29 / W ' nrs='0.29 / W ' sa=0 sb=0 sd=0 mult=1 m=1
XM4 net6 Vrefgate net7 VSS sky130_fd_pr__nfet_01v8 L=4 W='1 * 1 ' nf=1 ad='int((nf+1)/2) * W / nf * 0.29'
+ as='int((nf+2)/2) * W / nf * 0.29' pd='2*int((nf+1)/2) * (W / nf + 0.29)' ps='2*int((nf+2)/2) * (W / nf + 0.29)'
+ nrd='0.29 / W ' nrs='0.29 / W ' sa=0 sb=0 sd=0 mult=1 m=1
XMN5 net10 Vrefgate VSS VSS sky130_fd_pr__nfet_01v8_lvt L=4 W='1 * 1 ' nf=1 ad='int((nf+1)/2) * W / nf * 0.29'
+ as='int((nf+2)/2) * W / nf * 0.29' pd='2*int((nf+1)/2) * (W / nf + 0.29)' ps='2*int((nf+2)/2) * (W / nf + 0.29)'
+ nrd='0.29 / W ' nrs='0.29 / W ' sa=0 sb=0 sd=0 mult=1 m=1
XMN6 net14 Vrefgate net9 VSS sky130_fd_pr__nfet_01v8_lvt L=4 W='1 * 1 ' nf=1 ad='int((nf+1)/2) * W / nf * 0.29'
+ as='int((nf+2)/2) * W / nf * 0.29' pd='2*int((nf+1)/2) * (W / nf + 0.29)' ps='2*int((nf+2)/2) * (W / nf + 0.29)'
+ nrd='0.29 / W ' nrs='0.29 / W ' sa=0 sb=0 sd=0 mult=1 m=1
XMN9 net16 Vrefgate net14 VSS sky130_fd_pr__nfet_01v8_lvt L=4 W='1 * 1 ' nf=1 ad='int((nf+1)/2) * W / nf * 0.29'
+ as='int((nf+2)/2) * W / nf * 0.29' pd='2*int((nf+1)/2) * (W / nf + 0.29)' ps='2*int((nf+2)/2) * (W / nf + 0.29)'
+ nrd='0.29 / W ' nrs='0.29 / W ' sa=0 sb=0 sd=0 mult=1 m=1
XM5 Vrefgate Vrefgate net5 VSS sky130_fd_pr__nfet_01v8 L=4 W='1 * 1 ' nf=1 ad='int((nf+1)/2) * W / nf * 0.29'
+ as='int((nf+2)/2) * W / nf * 0.29' pd='2*int((nf+1)/2) * (W / nf + 0.29)' ps='2*int((nf+2)/2) * (W / nf + 0.29)'
+ nrd='0.29 / W ' nrs='0.29 / W ' sa=0 sb=0 sd=0 mult=1 m=1
XMN10 net11 Vrefgate net10 VSS sky130_fd_pr__nfet_01v8_lvt L=4 W='1 * 1 ' nf=1 ad='int((nf+1)/2) * W / nf * 0.29'
+ as='int((nf+2)/2) * W / nf * 0.29' pd='2*int((nf+1)/2) * (W / nf + 0.29)' ps='2*int((nf+2)/2) * (W / nf + 0.29)'
+ nrd='0.29 / W ' nrs='0.29 / W ' sa=0 sb=0 sd=0 mult=1 m=1
XMN11 net12 Vrefgate net11 VSS sky130_fd_pr__nfet_01v8_lvt L=4 W='1 * 1 ' nf=1 ad='int((nf+1)/2) * W / nf * 0.29'
+ as='int((nf+2)/2) * W / nf * 0.29' pd='2*int((nf+1)/2) * (W / nf + 0.29)' ps='2*int((nf+2)/2) * (W / nf + 0.29)'
+ nrd='0.29 / W ' nrs='0.29 / W ' sa=0 sb=0 sd=0 mult=1 m=1
XMN12 net13 Vrefgate net12 VSS sky130_fd_pr__nfet_01v8_lvt L=4 W='1 * 1 ' nf=1 ad='int((nf+1)/2) * W / nf * 0.29'
+ as='int((nf+2)/2) * W / nf * 0.29' pd='2*int((nf+1)/2) * (W / nf + 0.29)' ps='2*int((nf+2)/2) * (W / nf + 0.29)'
+ nrd='0.29 / W ' nrs='0.29 / W ' sa=0 sb=0 sd=0 mult=1 m=1
XMN13 net9 Vrefgate net13 VSS sky130_fd_pr__nfet_01v8_lvt L=4 W='1 * 1 ' nf=1 ad='int((nf+1)/2) * W / nf * 0.29'
+ as='int((nf+2)/2) * W / nf * 0.29' pd='2*int((nf+1)/2) * (W / nf + 0.29)' ps='2*int((nf+2)/2) * (W / nf + 0.29)'
+ nrd='0.29 / W ' nrs='0.29 / W ' sa=0 sb=0 sd=0 mult=1 m=1
XMN7 net18 Vrefgate net15 VSS sky130_fd_pr__nfet_01v8_lvt L=4 W='1 * 1 ' nf=1 ad='int((nf+1)/2) * W / nf * 0.29'
+ as='int((nf+2)/2) * W / nf * 0.29' pd='2*int((nf+1)/2) * (W / nf + 0.29)' ps='2*int((nf+2)/2) * (W / nf + 0.29)'
+ nrd='0.29 / W ' nrs='0.29 / W ' sa=0 sb=0 sd=0 mult=1 m=1
XMN8 Vref Vrefgate net18 VSS sky130_fd_pr__nfet_01v8_lvt L=4 W='1 * 1 ' nf=1 ad='int((nf+1)/2) * W / nf * 0.29'
+ as='int((nf+2)/2) * W / nf * 0.29' pd='2*int((nf+1)/2) * (W / nf + 0.29)' ps='2*int((nf+2)/2) * (W / nf + 0.29)'
+ nrd='0.29 / W ' nrs='0.29 / W ' sa=0 sb=0 sd=0 mult=1 m=1
XMN14 net17 Vrefgate net16 VSS sky130_fd_pr__nfet_01v8_lvt L=4 W='1 * 1 ' nf=1 ad='int((nf+1)/2) * W / nf * 0.29'
+ as='int((nf+2)/2) * W / nf * 0.29' pd='2*int((nf+1)/2) * (W / nf + 0.29)' ps='2*int((nf+2)/2) * (W / nf + 0.29)'
+ nrd='0.29 / W ' nrs='0.29 / W ' sa=0 sb=0 sd=0 mult=1 m=1
XMN15 net15 Vrefgate net17 VSS sky130_fd_pr__nfet_01v8_lvt L=4 W='1 * 1 ' nf=1 ad='int((nf+1)/2) * W / nf * 0.29'
+ as='int((nf+2)/2) * W / nf * 0.29' pd='2*int((nf+1)/2) * (W / nf + 0.29)' ps='2*int((nf+2)/2) * (W / nf + 0.29)'
+ nrd='0.29 / W ' nrs='0.29 / W ' sa=0 sb=0 sd=0 mult=1 m=1
XMP6 net19 VGP VDD VDD sky130_fd_pr__pfet_01v8_lvt L=8 W='0.55 * 7 ' nf=7 ad='int((nf+1)/2) * W / nf * 0.29'
+ as='int((nf+2)/2) * W / nf * 0.29' pd='2*int((nf+1)/2) * (W / nf + 0.29)' ps='2*int((nf+2)/2) * (W / nf + 0.29)'
+ nrd='0.29 / W ' nrs='0.29 / W ' sa=0 sb=0 sd=0 mult=1 m=1
XMN16 curr_n1 VGN net20 VSS sky130_fd_pr__nfet_01v8_lvt L=8 W='7 * 1 ' nf=1 ad='int((nf+1)/2) * W / nf * 0.29'
+ as='int((nf+2)/2) * W / nf * 0.29' pd='2*int((nf+1)/2) * (W / nf + 0.29)' ps='2*int((nf+2)/2) * (W / nf + 0.29)'
+ nrd='0.29 / W ' nrs='0.29 / W ' sa=0 sb=0 sd=0 mult=1 m=1
XMN17 net20 VGN VSS VSS sky130_fd_pr__nfet_01v8_lvt L=8 W='7 * 1 ' nf=1 ad='int((nf+1)/2) * W / nf * 0.29'
+ as='int((nf+2)/2) * W / nf * 0.29' pd='2*int((nf+1)/2) * (W / nf + 0.29)' ps='2*int((nf+2)/2) * (W / nf + 0.29)'
+ nrd='0.29 / W ' nrs='0.29 / W ' sa=0 sb=0 sd=0 mult=1 m=1
XM6 VGP vstartup VGN VSS sky130_fd_pr__nfet_01v8 L=4 W='1 * 1 ' nf=1 ad='int((nf+1)/2) * W / nf * 0.29'
+ as='int((nf+2)/2) * W / nf * 0.29' pd='2*int((nf+1)/2) * (W / nf + 0.29)' ps='2*int((nf+2)/2) * (W / nf + 0.29)'
+ nrd='0.29 / W ' nrs='0.29 / W ' sa=0 sb=0 sd=0 mult=1 m=1
XM7 vstartup Vrefgate VSS VSS sky130_fd_pr__nfet_01v8 L=4 W='1 * 1 ' nf=1 ad='int((nf+1)/2) * W / nf * 0.29'
+ as='int((nf+2)/2) * W / nf * 0.29' pd='2*int((nf+1)/2) * (W / nf + 0.29)' ps='2*int((nf+2)/2) * (W / nf + 0.29)'
+ nrd='0.29 / W ' nrs='0.29 / W ' sa=0 sb=0 sd=0 mult=1 m=1
XMN18 curr_n2 VGN net21 VSS sky130_fd_pr__nfet_01v8_lvt L=8 W='7 * 1 ' nf=1 ad='int((nf+1)/2) * W / nf * 0.29'
+ as='int((nf+2)/2) * W / nf * 0.29' pd='2*int((nf+1)/2) * (W / nf + 0.29)' ps='2*int((nf+2)/2) * (W / nf + 0.29)'
+ nrd='0.29 / W ' nrs='0.29 / W ' sa=0 sb=0 sd=0 mult=1 m=1
XMN19 net21 VGN VSS VSS sky130_fd_pr__nfet_01v8_lvt L=8 W='7 * 1 ' nf=1 ad='int((nf+1)/2) * W / nf * 0.29'
+ as='int((nf+2)/2) * W / nf * 0.29' pd='2*int((nf+1)/2) * (W / nf + 0.29)' ps='2*int((nf+2)/2) * (W / nf + 0.29)'
+ nrd='0.29 / W ' nrs='0.29 / W ' sa=0 sb=0 sd=0 mult=1 m=1
XC1 VDD vstartup sky130_fd_pr__cap_mim_m3_2 W=4 L=4 MF=1 m=1
.ends


* expanding   symbol:  ldo_fc_n.sym # of pins=10
** sym_path: xschem/ldo_fc_n.sym
** sch_path: xschem/ldo_fc_n.sch
.subckt ldo_fc_n VDD inp inn bias1 bias2 bias3 outn VSS bias4 comp
*.iopin VSS
*.iopin VDD
*.ipin inp
*.ipin inn
*.ipin bias1
*.opin outn
*.ipin bias2
*.ipin bias3
*.ipin bias4
*.opin comp
XMN4 outn bias3 net1 VSS sky130_fd_pr__nfet_01v8_lvt L=4 W='1 * 2 ' nf=2 ad='int((nf+1)/2) * W / nf * 0.29'
+ as='int((nf+2)/2) * W / nf * 0.29' pd='2*int((nf+1)/2) * (W / nf + 0.29)' ps='2*int((nf+2)/2) * (W / nf + 0.29)'
+ nrd='0.29 / W ' nrs='0.29 / W ' sa=0 sb=0 sd=0 mult=7 m=7
XMN7 net1 net3 net7 VSS sky130_fd_pr__nfet_01v8 L=8 W='0.42 * 4 ' nf=4 ad='int((nf+1)/2) * W / nf * 0.29'
+ as='int((nf+2)/2) * W / nf * 0.29' pd='2*int((nf+1)/2) * (W / nf + 0.29)' ps='2*int((nf+2)/2) * (W / nf + 0.29)'
+ nrd='0.29 / W ' nrs='0.29 / W ' sa=0 sb=0 sd=0 mult=7 m=7
XMN3 net3 bias3 net2 VSS sky130_fd_pr__nfet_01v8_lvt L=4 W='1 * 2 ' nf=2 ad='int((nf+1)/2) * W / nf * 0.29'
+ as='int((nf+2)/2) * W / nf * 0.29' pd='2*int((nf+1)/2) * (W / nf + 0.29)' ps='2*int((nf+2)/2) * (W / nf + 0.29)'
+ nrd='0.29 / W ' nrs='0.29 / W ' sa=0 sb=0 sd=0 mult=7 m=7
XMN6 net2 net3 net6 VSS sky130_fd_pr__nfet_01v8 L=8 W='0.42 * 4 ' nf=4 ad='int((nf+1)/2) * W / nf * 0.29'
+ as='int((nf+2)/2) * W / nf * 0.29' pd='2*int((nf+1)/2) * (W / nf + 0.29)' ps='2*int((nf+2)/2) * (W / nf + 0.29)'
+ nrd='0.29 / W ' nrs='0.29 / W ' sa=0 sb=0 sd=0 mult=7 m=7
XMP4 outn bias2 comp VDD sky130_fd_pr__pfet_01v8_lvt L=8 W='0.55 * 4 ' nf=4 ad='int((nf+1)/2) * W / nf * 0.29'
+ as='int((nf+2)/2) * W / nf * 0.29' pd='2*int((nf+1)/2) * (W / nf + 0.29)' ps='2*int((nf+2)/2) * (W / nf + 0.29)'
+ nrd='0.29 / W ' nrs='0.29 / W ' sa=0 sb=0 sd=0 mult=7 m=7
XMP2 comp bias1 VDD VDD sky130_fd_pr__pfet_01v8_lvt L=8 W='0.55 * 4 ' nf=4 ad='int((nf+1)/2) * W / nf * 0.29'
+ as='int((nf+2)/2) * W / nf * 0.29' pd='2*int((nf+1)/2) * (W / nf + 0.29)' ps='2*int((nf+2)/2) * (W / nf + 0.29)'
+ nrd='0.29 / W ' nrs='0.29 / W ' sa=0 sb=0 sd=0 mult=11 m=11
XMP3 net3 bias2 net4 VDD sky130_fd_pr__pfet_01v8_lvt L=8 W='0.55 * 4 ' nf=4 ad='int((nf+1)/2) * W / nf * 0.29'
+ as='int((nf+2)/2) * W / nf * 0.29' pd='2*int((nf+1)/2) * (W / nf + 0.29)' ps='2*int((nf+2)/2) * (W / nf + 0.29)'
+ nrd='0.29 / W ' nrs='0.29 / W ' sa=0 sb=0 sd=0 mult=7 m=7
XMP1 net4 bias1 VDD VDD sky130_fd_pr__pfet_01v8_lvt L=8 W='0.55 * 4 ' nf=4 ad='int((nf+1)/2) * W / nf * 0.29'
+ as='int((nf+2)/2) * W / nf * 0.29' pd='2*int((nf+1)/2) * (W / nf + 0.29)' ps='2*int((nf+2)/2) * (W / nf + 0.29)'
+ nrd='0.29 / W ' nrs='0.29 / W ' sa=0 sb=0 sd=0 mult=11 m=11
XMN5 net5 bias4 net8 VSS sky130_fd_pr__nfet_01v8 L=8 W='0.42 * 4 ' nf=4 ad='int((nf+1)/2) * W / nf * 0.29'
+ as='int((nf+2)/2) * W / nf * 0.29' pd='2*int((nf+1)/2) * (W / nf + 0.29)' ps='2*int((nf+2)/2) * (W / nf + 0.29)'
+ nrd='0.29 / W ' nrs='0.29 / W ' sa=0 sb=0 sd=0 mult=8 m=8
XMN1 net4 inn net5 VSS sky130_fd_pr__nfet_01v8_lvt L=4 W='1 * 1 ' nf=1 ad='int((nf+1)/2) * W / nf * 0.29'
+ as='int((nf+2)/2) * W / nf * 0.29' pd='2*int((nf+1)/2) * (W / nf + 0.29)' ps='2*int((nf+2)/2) * (W / nf + 0.29)'
+ nrd='0.29 / W ' nrs='0.29 / W ' sa=0 sb=0 sd=0 mult=1 m=1
XMN2 comp inp net5 VSS sky130_fd_pr__nfet_01v8_lvt L=4 W='1 * 1 ' nf=1 ad='int((nf+1)/2) * W / nf * 0.29'
+ as='int((nf+2)/2) * W / nf * 0.29' pd='2*int((nf+1)/2) * (W / nf + 0.29)' ps='2*int((nf+2)/2) * (W / nf + 0.29)'
+ nrd='0.29 / W ' nrs='0.29 / W ' sa=0 sb=0 sd=0 mult=1 m=1
XMN9 net7 net3 net9 VSS sky130_fd_pr__nfet_01v8 L=8 W='0.42 * 4 ' nf=4 ad='int((nf+1)/2) * W / nf * 0.29'
+ as='int((nf+2)/2) * W / nf * 0.29' pd='2*int((nf+1)/2) * (W / nf + 0.29)' ps='2*int((nf+2)/2) * (W / nf + 0.29)'
+ nrd='0.29 / W ' nrs='0.29 / W ' sa=0 sb=0 sd=0 mult=7 m=7
XMN10 net6 net3 net10 VSS sky130_fd_pr__nfet_01v8 L=8 W='0.42 * 4 ' nf=4 ad='int((nf+1)/2) * W / nf * 0.29'
+ as='int((nf+2)/2) * W / nf * 0.29' pd='2*int((nf+1)/2) * (W / nf + 0.29)' ps='2*int((nf+2)/2) * (W / nf + 0.29)'
+ nrd='0.29 / W ' nrs='0.29 / W ' sa=0 sb=0 sd=0 mult=7 m=7
XMN11 net8 bias4 net11 VSS sky130_fd_pr__nfet_01v8 L=8 W='0.42 * 4 ' nf=4 ad='int((nf+1)/2) * W / nf * 0.29'
+ as='int((nf+2)/2) * W / nf * 0.29' pd='2*int((nf+1)/2) * (W / nf + 0.29)' ps='2*int((nf+2)/2) * (W / nf + 0.29)'
+ nrd='0.29 / W ' nrs='0.29 / W ' sa=0 sb=0 sd=0 mult=8 m=8
XMN8 net9 net3 net12 VSS sky130_fd_pr__nfet_01v8 L=8 W='0.42 * 4 ' nf=4 ad='int((nf+1)/2) * W / nf * 0.29'
+ as='int((nf+2)/2) * W / nf * 0.29' pd='2*int((nf+1)/2) * (W / nf + 0.29)' ps='2*int((nf+2)/2) * (W / nf + 0.29)'
+ nrd='0.29 / W ' nrs='0.29 / W ' sa=0 sb=0 sd=0 mult=7 m=7
XMN12 net10 net3 net14 VSS sky130_fd_pr__nfet_01v8 L=8 W='0.42 * 4 ' nf=4 ad='int((nf+1)/2) * W / nf * 0.29'
+ as='int((nf+2)/2) * W / nf * 0.29' pd='2*int((nf+1)/2) * (W / nf + 0.29)' ps='2*int((nf+2)/2) * (W / nf + 0.29)'
+ nrd='0.29 / W ' nrs='0.29 / W ' sa=0 sb=0 sd=0 mult=7 m=7
XMN13 net11 bias4 net13 VSS sky130_fd_pr__nfet_01v8 L=8 W='0.42 * 4 ' nf=4 ad='int((nf+1)/2) * W / nf * 0.29'
+ as='int((nf+2)/2) * W / nf * 0.29' pd='2*int((nf+1)/2) * (W / nf + 0.29)' ps='2*int((nf+2)/2) * (W / nf + 0.29)'
+ nrd='0.29 / W ' nrs='0.29 / W ' sa=0 sb=0 sd=0 mult=8 m=8
XMN14 net12 net3 VSS VSS sky130_fd_pr__nfet_01v8 L=8 W='0.42 * 4 ' nf=4 ad='int((nf+1)/2) * W / nf * 0.29'
+ as='int((nf+2)/2) * W / nf * 0.29' pd='2*int((nf+1)/2) * (W / nf + 0.29)' ps='2*int((nf+2)/2) * (W / nf + 0.29)'
+ nrd='0.29 / W ' nrs='0.29 / W ' sa=0 sb=0 sd=0 mult=7 m=7
XMN15 net14 net3 VSS VSS sky130_fd_pr__nfet_01v8 L=8 W='0.42 * 4 ' nf=4 ad='int((nf+1)/2) * W / nf * 0.29'
+ as='int((nf+2)/2) * W / nf * 0.29' pd='2*int((nf+1)/2) * (W / nf + 0.29)' ps='2*int((nf+2)/2) * (W / nf + 0.29)'
+ nrd='0.29 / W ' nrs='0.29 / W ' sa=0 sb=0 sd=0 mult=7 m=7
XMN16 net13 bias4 VSS VSS sky130_fd_pr__nfet_01v8 L=8 W='0.42 * 4 ' nf=4 ad='int((nf+1)/2) * W / nf * 0.29'
+ as='int((nf+2)/2) * W / nf * 0.29' pd='2*int((nf+1)/2) * (W / nf + 0.29)' ps='2*int((nf+2)/2) * (W / nf + 0.29)'
+ nrd='0.29 / W ' nrs='0.29 / W ' sa=0 sb=0 sd=0 mult=8 m=8
.ends

.GLOBAL GND
.end
